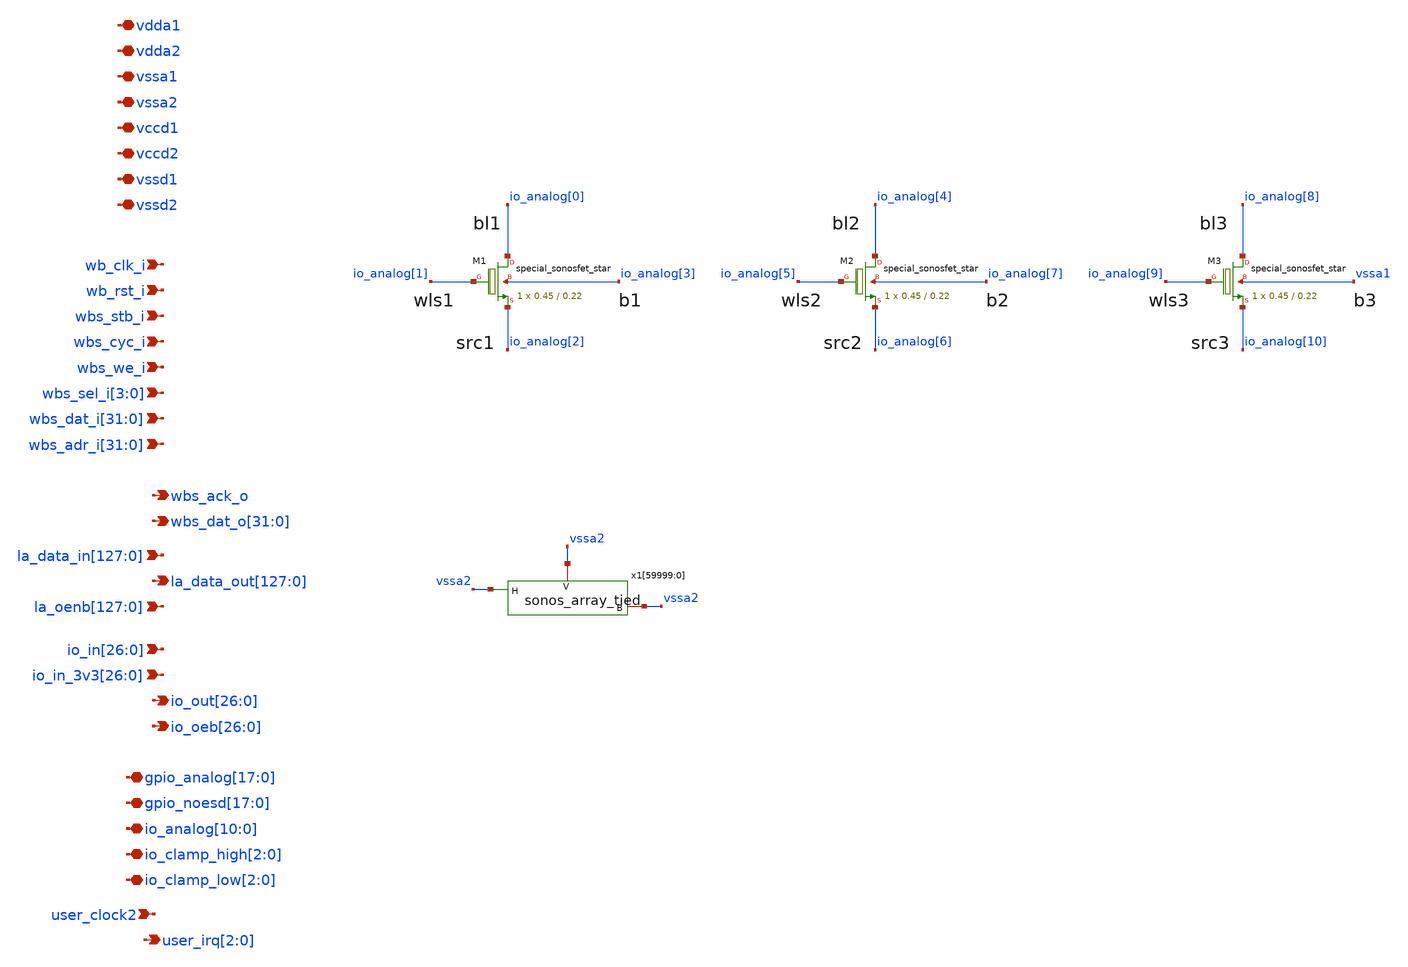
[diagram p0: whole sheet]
** sch_path: xschem/user_analog_project_wrapper.sch
**.subckt user_analog_project_wrapper vdda1 vdda2 vssa1 vssa2 vccd1 vccd2 vssd1 vssd2 wb_clk_i
*+ wb_rst_i wbs_stb_i wbs_cyc_i wbs_we_i wbs_sel_i[3],wbs_sel_i[2],wbs_sel_i[1],wbs_sel_i[0]
*+ wbs_dat_i[31],wbs_dat_i[30],wbs_dat_i[29],wbs_dat_i[28],wbs_dat_i[27],wbs_dat_i[26],wbs_dat_i[25],wbs_dat_i[24],wbs_dat_i[23],wbs_dat_i[22],wbs_dat_i[21],wbs_dat_i[20],wbs_dat_i[19],wbs_dat_i[18],wbs_dat_i[17],wbs_dat_i[16],wbs_dat_i[15],wbs_dat_i[14],wbs_dat_i[13],wbs_dat_i[12],wbs_dat_i[11],wbs_dat_i[10],wbs_dat_i[9],wbs_dat_i[8],wbs_dat_i[7],wbs_dat_i[6],wbs_dat_i[5],wbs_dat_i[4],wbs_dat_i[3],wbs_dat_i[2],wbs_dat_i[1],wbs_dat_i[0]
*+ wbs_adr_i[31],wbs_adr_i[30],wbs_adr_i[29],wbs_adr_i[28],wbs_adr_i[27],wbs_adr_i[26],wbs_adr_i[25],wbs_adr_i[24],wbs_adr_i[23],wbs_adr_i[22],wbs_adr_i[21],wbs_adr_i[20],wbs_adr_i[19],wbs_adr_i[18],wbs_adr_i[17],wbs_adr_i[16],wbs_adr_i[15],wbs_adr_i[14],wbs_adr_i[13],wbs_adr_i[12],wbs_adr_i[11],wbs_adr_i[10],wbs_adr_i[9],wbs_adr_i[8],wbs_adr_i[7],wbs_adr_i[6],wbs_adr_i[5],wbs_adr_i[4],wbs_adr_i[3],wbs_adr_i[2],wbs_adr_i[1],wbs_adr_i[0] wbs_ack_o
*+ wbs_dat_o[31],wbs_dat_o[30],wbs_dat_o[29],wbs_dat_o[28],wbs_dat_o[27],wbs_dat_o[26],wbs_dat_o[25],wbs_dat_o[24],wbs_dat_o[23],wbs_dat_o[22],wbs_dat_o[21],wbs_dat_o[20],wbs_dat_o[19],wbs_dat_o[18],wbs_dat_o[17],wbs_dat_o[16],wbs_dat_o[15],wbs_dat_o[14],wbs_dat_o[13],wbs_dat_o[12],wbs_dat_o[11],wbs_dat_o[10],wbs_dat_o[9],wbs_dat_o[8],wbs_dat_o[7],wbs_dat_o[6],wbs_dat_o[5],wbs_dat_o[4],wbs_dat_o[3],wbs_dat_o[2],wbs_dat_o[1],wbs_dat_o[0]
*+ la_data_in[127],la_data_in[126],la_data_in[125],la_data_in[124],la_data_in[123],la_data_in[122],la_data_in[121],la_data_in[120],la_data_in[119],la_data_in[118],la_data_in[117],la_data_in[116],la_data_in[115],la_data_in[114],la_data_in[113],la_data_in[112],la_data_in[111],la_data_in[110],la_data_in[109],la_data_in[108],la_data_in[107],la_data_in[106],la_data_in[105],la_data_in[104],la_data_in[103],la_data_in[102],la_data_in[101],la_data_in[100],la_data_in[99],la_data_in[98],la_data_in[97],la_data_in[96],la_data_in[95],la_data_in[94],la_data_in[93],la_data_in[92],la_data_in[91],la_data_in[90],la_data_in[89],la_data_in[88],la_data_in[87],la_data_in[86],la_data_in[85],la_data_in[84],la_data_in[83],la_data_in[82],la_data_in[81],la_data_in[80],la_data_in[79],la_data_in[78],la_data_in[77],la_data_in[76],la_data_in[75],la_data_in[74],la_data_in[73],la_data_in[72],la_data_in[71],la_data_in[70],la_data_in[69],la_data_in[68],la_data_in[67],la_data_in[66],la_data_in[65],la_data_in[64],la_data_in[63],la_data_in[62],la_data_in[61],la_data_in[60],la_data_in[59],la_data_in[58],la_data_in[57],la_data_in[56],la_data_in[55],la_data_in[54],la_data_in[53],la_data_in[52],la_data_in[51],la_data_in[50],la_data_in[49],la_data_in[48],la_data_in[47],la_data_in[46],la_data_in[45],la_data_in[44],la_data_in[43],la_data_in[42],la_data_in[41],la_data_in[40],la_data_in[39],la_data_in[38],la_data_in[37],la_data_in[36],la_data_in[35],la_data_in[34],la_data_in[33],la_data_in[32],la_data_in[31],la_data_in[30],la_data_in[29],la_data_in[28],la_data_in[27],la_data_in[26],la_data_in[25],la_data_in[24],la_data_in[23],la_data_in[22],la_data_in[21],la_data_in[20],la_data_in[19],la_data_in[18],la_data_in[17],la_data_in[16],la_data_in[15],la_data_in[14],la_data_in[13],la_data_in[12],la_data_in[11],la_data_in[10],la_data_in[9],la_data_in[8],la_data_in[7],la_data_in[6],la_data_in[5],la_data_in[4],la_data_in[3],la_data_in[2],la_data_in[1],la_data_in[0]
*+ la_data_out[127],la_data_out[126],la_data_out[125],la_data_out[124],la_data_out[123],la_data_out[122],la_data_out[121],la_data_out[120],la_data_out[119],la_data_out[118],la_data_out[117],la_data_out[116],la_data_out[115],la_data_out[114],la_data_out[113],la_data_out[112],la_data_out[111],la_data_out[110],la_data_out[109],la_data_out[108],la_data_out[107],la_data_out[106],la_data_out[105],la_data_out[104],la_data_out[103],la_data_out[102],la_data_out[101],la_data_out[100],la_data_out[99],la_data_out[98],la_data_out[97],la_data_out[96],la_data_out[95],la_data_out[94],la_data_out[93],la_data_out[92],la_data_out[91],la_data_out[90],la_data_out[89],la_data_out[88],la_data_out[87],la_data_out[86],la_data_out[85],la_data_out[84],la_data_out[83],la_data_out[82],la_data_out[81],la_data_out[80],la_data_out[79],la_data_out[78],la_data_out[77],la_data_out[76],la_data_out[75],la_data_out[74],la_data_out[73],la_data_out[72],la_data_out[71],la_data_out[70],la_data_out[69],la_data_out[68],la_data_out[67],la_data_out[66],la_data_out[65],la_data_out[64],la_data_out[63],la_data_out[62],la_data_out[61],la_data_out[60],la_data_out[59],la_data_out[58],la_data_out[57],la_data_out[56],la_data_out[55],la_data_out[54],la_data_out[53],la_data_out[52],la_data_out[51],la_data_out[50],la_data_out[49],la_data_out[48],la_data_out[47],la_data_out[46],la_data_out[45],la_data_out[44],la_data_out[43],la_data_out[42],la_data_out[41],la_data_out[40],la_data_out[39],la_data_out[38],la_data_out[37],la_data_out[36],la_data_out[35],la_data_out[34],la_data_out[33],la_data_out[32],la_data_out[31],la_data_out[30],la_data_out[29],la_data_out[28],la_data_out[27],la_data_out[26],la_data_out[25],la_data_out[24],la_data_out[23],la_data_out[22],la_data_out[21],la_data_out[20],la_data_out[19],la_data_out[18],la_data_out[17],la_data_out[16],la_data_out[15],la_data_out[14],la_data_out[13],la_data_out[12],la_data_out[11],la_data_out[10],la_data_out[9],la_data_out[8],la_data_out[7],la_data_out[6],la_data_out[5],la_data_out[4],la_data_out[3],la_data_out[2],la_data_out[1],la_data_out[0]
*+ io_in[26],io_in[25],io_in[24],io_in[23],io_in[22],io_in[21],io_in[20],io_in[19],io_in[18],io_in[17],io_in[16],io_in[15],io_in[14],io_in[13],io_in[12],io_in[11],io_in[10],io_in[9],io_in[8],io_in[7],io_in[6],io_in[5],io_in[4],io_in[3],io_in[2],io_in[1],io_in[0]
*+ io_in_3v3[26],io_in_3v3[25],io_in_3v3[24],io_in_3v3[23],io_in_3v3[22],io_in_3v3[21],io_in_3v3[20],io_in_3v3[19],io_in_3v3[18],io_in_3v3[17],io_in_3v3[16],io_in_3v3[15],io_in_3v3[14],io_in_3v3[13],io_in_3v3[12],io_in_3v3[11],io_in_3v3[10],io_in_3v3[9],io_in_3v3[8],io_in_3v3[7],io_in_3v3[6],io_in_3v3[5],io_in_3v3[4],io_in_3v3[3],io_in_3v3[2],io_in_3v3[1],io_in_3v3[0] user_clock2
*+ io_out[26],io_out[25],io_out[24],io_out[23],io_out[22],io_out[21],io_out[20],io_out[19],io_out[18],io_out[17],io_out[16],io_out[15],io_out[14],io_out[13],io_out[12],io_out[11],io_out[10],io_out[9],io_out[8],io_out[7],io_out[6],io_out[5],io_out[4],io_out[3],io_out[2],io_out[1],io_out[0]
*+ io_oeb[26],io_oeb[25],io_oeb[24],io_oeb[23],io_oeb[22],io_oeb[21],io_oeb[20],io_oeb[19],io_oeb[18],io_oeb[17],io_oeb[16],io_oeb[15],io_oeb[14],io_oeb[13],io_oeb[12],io_oeb[11],io_oeb[10],io_oeb[9],io_oeb[8],io_oeb[7],io_oeb[6],io_oeb[5],io_oeb[4],io_oeb[3],io_oeb[2],io_oeb[1],io_oeb[0]
*+ gpio_analog[17],gpio_analog[16],gpio_analog[15],gpio_analog[14],gpio_analog[13],gpio_analog[12],gpio_analog[11],gpio_analog[10],gpio_analog[9],gpio_analog[8],gpio_analog[7],gpio_analog[6],gpio_analog[5],gpio_analog[4],gpio_analog[3],gpio_analog[2],gpio_analog[1],gpio_analog[0]
*+ gpio_noesd[17],gpio_noesd[16],gpio_noesd[15],gpio_noesd[14],gpio_noesd[13],gpio_noesd[12],gpio_noesd[11],gpio_noesd[10],gpio_noesd[9],gpio_noesd[8],gpio_noesd[7],gpio_noesd[6],gpio_noesd[5],gpio_noesd[4],gpio_noesd[3],gpio_noesd[2],gpio_noesd[1],gpio_noesd[0]
*+ io_analog[10],io_analog[9],io_analog[8],io_analog[7],io_analog[6],io_analog[5],io_analog[4],io_analog[3],io_analog[2],io_analog[1],io_analog[0] io_clamp_high[2],io_clamp_high[1],io_clamp_high[0] io_clamp_low[2],io_clamp_low[1],io_clamp_low[0]
*+ user_irq[2],user_irq[1],user_irq[0]
*+ la_oenb[127],la_oenb[126],la_oenb[125],la_oenb[124],la_oenb[123],la_oenb[122],la_oenb[121],la_oenb[120],la_oenb[119],la_oenb[118],la_oenb[117],la_oenb[116],la_oenb[115],la_oenb[114],la_oenb[113],la_oenb[112],la_oenb[111],la_oenb[110],la_oenb[109],la_oenb[108],la_oenb[107],la_oenb[106],la_oenb[105],la_oenb[104],la_oenb[103],la_oenb[102],la_oenb[101],la_oenb[100],la_oenb[99],la_oenb[98],la_oenb[97],la_oenb[96],la_oenb[95],la_oenb[94],la_oenb[93],la_oenb[92],la_oenb[91],la_oenb[90],la_oenb[89],la_oenb[88],la_oenb[87],la_oenb[86],la_oenb[85],la_oenb[84],la_oenb[83],la_oenb[82],la_oenb[81],la_oenb[80],la_oenb[79],la_oenb[78],la_oenb[77],la_oenb[76],la_oenb[75],la_oenb[74],la_oenb[73],la_oenb[72],la_oenb[71],la_oenb[70],la_oenb[69],la_oenb[68],la_oenb[67],la_oenb[66],la_oenb[65],la_oenb[64],la_oenb[63],la_oenb[62],la_oenb[61],la_oenb[60],la_oenb[59],la_oenb[58],la_oenb[57],la_oenb[56],la_oenb[55],la_oenb[54],la_oenb[53],la_oenb[52],la_oenb[51],la_oenb[50],la_oenb[49],la_oenb[48],la_oenb[47],la_oenb[46],la_oenb[45],la_oenb[44],la_oenb[43],la_oenb[42],la_oenb[41],la_oenb[40],la_oenb[39],la_oenb[38],la_oenb[37],la_oenb[36],la_oenb[35],la_oenb[34],la_oenb[33],la_oenb[32],la_oenb[31],la_oenb[30],la_oenb[29],la_oenb[28],la_oenb[27],la_oenb[26],la_oenb[25],la_oenb[24],la_oenb[23],la_oenb[22],la_oenb[21],la_oenb[20],la_oenb[19],la_oenb[18],la_oenb[17],la_oenb[16],la_oenb[15],la_oenb[14],la_oenb[13],la_oenb[12],la_oenb[11],la_oenb[10],la_oenb[9],la_oenb[8],la_oenb[7],la_oenb[6],la_oenb[5],la_oenb[4],la_oenb[3],la_oenb[2],la_oenb[1],la_oenb[0]
*.iopin vdda1
*.iopin vdda2
*.iopin vssa1
*.iopin vssa2
*.iopin vccd1
*.iopin vccd2
*.iopin vssd1
*.iopin vssd2
*.ipin wb_clk_i
*.ipin wb_rst_i
*.ipin wbs_stb_i
*.ipin wbs_cyc_i
*.ipin wbs_we_i
*.ipin wbs_sel_i[3],wbs_sel_i[2],wbs_sel_i[1],wbs_sel_i[0]
*.ipin
*+ wbs_dat_i[31],wbs_dat_i[30],wbs_dat_i[29],wbs_dat_i[28],wbs_dat_i[27],wbs_dat_i[26],wbs_dat_i[25],wbs_dat_i[24],wbs_dat_i[23],wbs_dat_i[22],wbs_dat_i[21],wbs_dat_i[20],wbs_dat_i[19],wbs_dat_i[18],wbs_dat_i[17],wbs_dat_i[16],wbs_dat_i[15],wbs_dat_i[14],wbs_dat_i[13],wbs_dat_i[12],wbs_dat_i[11],wbs_dat_i[10],wbs_dat_i[9],wbs_dat_i[8],wbs_dat_i[7],wbs_dat_i[6],wbs_dat_i[5],wbs_dat_i[4],wbs_dat_i[3],wbs_dat_i[2],wbs_dat_i[1],wbs_dat_i[0]
*.ipin
*+ wbs_adr_i[31],wbs_adr_i[30],wbs_adr_i[29],wbs_adr_i[28],wbs_adr_i[27],wbs_adr_i[26],wbs_adr_i[25],wbs_adr_i[24],wbs_adr_i[23],wbs_adr_i[22],wbs_adr_i[21],wbs_adr_i[20],wbs_adr_i[19],wbs_adr_i[18],wbs_adr_i[17],wbs_adr_i[16],wbs_adr_i[15],wbs_adr_i[14],wbs_adr_i[13],wbs_adr_i[12],wbs_adr_i[11],wbs_adr_i[10],wbs_adr_i[9],wbs_adr_i[8],wbs_adr_i[7],wbs_adr_i[6],wbs_adr_i[5],wbs_adr_i[4],wbs_adr_i[3],wbs_adr_i[2],wbs_adr_i[1],wbs_adr_i[0]
*.opin wbs_ack_o
*.opin
*+ wbs_dat_o[31],wbs_dat_o[30],wbs_dat_o[29],wbs_dat_o[28],wbs_dat_o[27],wbs_dat_o[26],wbs_dat_o[25],wbs_dat_o[24],wbs_dat_o[23],wbs_dat_o[22],wbs_dat_o[21],wbs_dat_o[20],wbs_dat_o[19],wbs_dat_o[18],wbs_dat_o[17],wbs_dat_o[16],wbs_dat_o[15],wbs_dat_o[14],wbs_dat_o[13],wbs_dat_o[12],wbs_dat_o[11],wbs_dat_o[10],wbs_dat_o[9],wbs_dat_o[8],wbs_dat_o[7],wbs_dat_o[6],wbs_dat_o[5],wbs_dat_o[4],wbs_dat_o[3],wbs_dat_o[2],wbs_dat_o[1],wbs_dat_o[0]
*.ipin
*+ la_data_in[127],la_data_in[126],la_data_in[125],la_data_in[124],la_data_in[123],la_data_in[122],la_data_in[121],la_data_in[120],la_data_in[119],la_data_in[118],la_data_in[117],la_data_in[116],la_data_in[115],la_data_in[114],la_data_in[113],la_data_in[112],la_data_in[111],la_data_in[110],la_data_in[109],la_data_in[108],la_data_in[107],la_data_in[106],la_data_in[105],la_data_in[104],la_data_in[103],la_data_in[102],la_data_in[101],la_data_in[100],la_data_in[99],la_data_in[98],la_data_in[97],la_data_in[96],la_data_in[95],la_data_in[94],la_data_in[93],la_data_in[92],la_data_in[91],la_data_in[90],la_data_in[89],la_data_in[88],la_data_in[87],la_data_in[86],la_data_in[85],la_data_in[84],la_data_in[83],la_data_in[82],la_data_in[81],la_data_in[80],la_data_in[79],la_data_in[78],la_data_in[77],la_data_in[76],la_data_in[75],la_data_in[74],la_data_in[73],la_data_in[72],la_data_in[71],la_data_in[70],la_data_in[69],la_data_in[68],la_data_in[67],la_data_in[66],la_data_in[65],la_data_in[64],la_data_in[63],la_data_in[62],la_data_in[61],la_data_in[60],la_data_in[59],la_data_in[58],la_data_in[57],la_data_in[56],la_data_in[55],la_data_in[54],la_data_in[53],la_data_in[52],la_data_in[51],la_data_in[50],la_data_in[49],la_data_in[48],la_data_in[47],la_data_in[46],la_data_in[45],la_data_in[44],la_data_in[43],la_data_in[42],la_data_in[41],la_data_in[40],la_data_in[39],la_data_in[38],la_data_in[37],la_data_in[36],la_data_in[35],la_data_in[34],la_data_in[33],la_data_in[32],la_data_in[31],la_data_in[30],la_data_in[29],la_data_in[28],la_data_in[27],la_data_in[26],la_data_in[25],la_data_in[24],la_data_in[23],la_data_in[22],la_data_in[21],la_data_in[20],la_data_in[19],la_data_in[18],la_data_in[17],la_data_in[16],la_data_in[15],la_data_in[14],la_data_in[13],la_data_in[12],la_data_in[11],la_data_in[10],la_data_in[9],la_data_in[8],la_data_in[7],la_data_in[6],la_data_in[5],la_data_in[4],la_data_in[3],la_data_in[2],la_data_in[1],la_data_in[0]
*.opin
*+ la_data_out[127],la_data_out[126],la_data_out[125],la_data_out[124],la_data_out[123],la_data_out[122],la_data_out[121],la_data_out[120],la_data_out[119],la_data_out[118],la_data_out[117],la_data_out[116],la_data_out[115],la_data_out[114],la_data_out[113],la_data_out[112],la_data_out[111],la_data_out[110],la_data_out[109],la_data_out[108],la_data_out[107],la_data_out[106],la_data_out[105],la_data_out[104],la_data_out[103],la_data_out[102],la_data_out[101],la_data_out[100],la_data_out[99],la_data_out[98],la_data_out[97],la_data_out[96],la_data_out[95],la_data_out[94],la_data_out[93],la_data_out[92],la_data_out[91],la_data_out[90],la_data_out[89],la_data_out[88],la_data_out[87],la_data_out[86],la_data_out[85],la_data_out[84],la_data_out[83],la_data_out[82],la_data_out[81],la_data_out[80],la_data_out[79],la_data_out[78],la_data_out[77],la_data_out[76],la_data_out[75],la_data_out[74],la_data_out[73],la_data_out[72],la_data_out[71],la_data_out[70],la_data_out[69],la_data_out[68],la_data_out[67],la_data_out[66],la_data_out[65],la_data_out[64],la_data_out[63],la_data_out[62],la_data_out[61],la_data_out[60],la_data_out[59],la_data_out[58],la_data_out[57],la_data_out[56],la_data_out[55],la_data_out[54],la_data_out[53],la_data_out[52],la_data_out[51],la_data_out[50],la_data_out[49],la_data_out[48],la_data_out[47],la_data_out[46],la_data_out[45],la_data_out[44],la_data_out[43],la_data_out[42],la_data_out[41],la_data_out[40],la_data_out[39],la_data_out[38],la_data_out[37],la_data_out[36],la_data_out[35],la_data_out[34],la_data_out[33],la_data_out[32],la_data_out[31],la_data_out[30],la_data_out[29],la_data_out[28],la_data_out[27],la_data_out[26],la_data_out[25],la_data_out[24],la_data_out[23],la_data_out[22],la_data_out[21],la_data_out[20],la_data_out[19],la_data_out[18],la_data_out[17],la_data_out[16],la_data_out[15],la_data_out[14],la_data_out[13],la_data_out[12],la_data_out[11],la_data_out[10],la_data_out[9],la_data_out[8],la_data_out[7],la_data_out[6],la_data_out[5],la_data_out[4],la_data_out[3],la_data_out[2],la_data_out[1],la_data_out[0]
*.ipin
*+ io_in[26],io_in[25],io_in[24],io_in[23],io_in[22],io_in[21],io_in[20],io_in[19],io_in[18],io_in[17],io_in[16],io_in[15],io_in[14],io_in[13],io_in[12],io_in[11],io_in[10],io_in[9],io_in[8],io_in[7],io_in[6],io_in[5],io_in[4],io_in[3],io_in[2],io_in[1],io_in[0]
*.ipin
*+ io_in_3v3[26],io_in_3v3[25],io_in_3v3[24],io_in_3v3[23],io_in_3v3[22],io_in_3v3[21],io_in_3v3[20],io_in_3v3[19],io_in_3v3[18],io_in_3v3[17],io_in_3v3[16],io_in_3v3[15],io_in_3v3[14],io_in_3v3[13],io_in_3v3[12],io_in_3v3[11],io_in_3v3[10],io_in_3v3[9],io_in_3v3[8],io_in_3v3[7],io_in_3v3[6],io_in_3v3[5],io_in_3v3[4],io_in_3v3[3],io_in_3v3[2],io_in_3v3[1],io_in_3v3[0]
*.ipin user_clock2
*.opin
*+ io_out[26],io_out[25],io_out[24],io_out[23],io_out[22],io_out[21],io_out[20],io_out[19],io_out[18],io_out[17],io_out[16],io_out[15],io_out[14],io_out[13],io_out[12],io_out[11],io_out[10],io_out[9],io_out[8],io_out[7],io_out[6],io_out[5],io_out[4],io_out[3],io_out[2],io_out[1],io_out[0]
*.opin
*+ io_oeb[26],io_oeb[25],io_oeb[24],io_oeb[23],io_oeb[22],io_oeb[21],io_oeb[20],io_oeb[19],io_oeb[18],io_oeb[17],io_oeb[16],io_oeb[15],io_oeb[14],io_oeb[13],io_oeb[12],io_oeb[11],io_oeb[10],io_oeb[9],io_oeb[8],io_oeb[7],io_oeb[6],io_oeb[5],io_oeb[4],io_oeb[3],io_oeb[2],io_oeb[1],io_oeb[0]
*.iopin
*+ gpio_analog[17],gpio_analog[16],gpio_analog[15],gpio_analog[14],gpio_analog[13],gpio_analog[12],gpio_analog[11],gpio_analog[10],gpio_analog[9],gpio_analog[8],gpio_analog[7],gpio_analog[6],gpio_analog[5],gpio_analog[4],gpio_analog[3],gpio_analog[2],gpio_analog[1],gpio_analog[0]
*.iopin
*+ gpio_noesd[17],gpio_noesd[16],gpio_noesd[15],gpio_noesd[14],gpio_noesd[13],gpio_noesd[12],gpio_noesd[11],gpio_noesd[10],gpio_noesd[9],gpio_noesd[8],gpio_noesd[7],gpio_noesd[6],gpio_noesd[5],gpio_noesd[4],gpio_noesd[3],gpio_noesd[2],gpio_noesd[1],gpio_noesd[0]
*.iopin
*+ io_analog[10],io_analog[9],io_analog[8],io_analog[7],io_analog[6],io_analog[5],io_analog[4],io_analog[3],io_analog[2],io_analog[1],io_analog[0]
*.iopin io_clamp_high[2],io_clamp_high[1],io_clamp_high[0]
*.iopin io_clamp_low[2],io_clamp_low[1],io_clamp_low[0]
*.opin user_irq[2],user_irq[1],user_irq[0]
*.ipin
*+ la_oenb[127],la_oenb[126],la_oenb[125],la_oenb[124],la_oenb[123],la_oenb[122],la_oenb[121],la_oenb[120],la_oenb[119],la_oenb[118],la_oenb[117],la_oenb[116],la_oenb[115],la_oenb[114],la_oenb[113],la_oenb[112],la_oenb[111],la_oenb[110],la_oenb[109],la_oenb[108],la_oenb[107],la_oenb[106],la_oenb[105],la_oenb[104],la_oenb[103],la_oenb[102],la_oenb[101],la_oenb[100],la_oenb[99],la_oenb[98],la_oenb[97],la_oenb[96],la_oenb[95],la_oenb[94],la_oenb[93],la_oenb[92],la_oenb[91],la_oenb[90],la_oenb[89],la_oenb[88],la_oenb[87],la_oenb[86],la_oenb[85],la_oenb[84],la_oenb[83],la_oenb[82],la_oenb[81],la_oenb[80],la_oenb[79],la_oenb[78],la_oenb[77],la_oenb[76],la_oenb[75],la_oenb[74],la_oenb[73],la_oenb[72],la_oenb[71],la_oenb[70],la_oenb[69],la_oenb[68],la_oenb[67],la_oenb[66],la_oenb[65],la_oenb[64],la_oenb[63],la_oenb[62],la_oenb[61],la_oenb[60],la_oenb[59],la_oenb[58],la_oenb[57],la_oenb[56],la_oenb[55],la_oenb[54],la_oenb[53],la_oenb[52],la_oenb[51],la_oenb[50],la_oenb[49],la_oenb[48],la_oenb[47],la_oenb[46],la_oenb[45],la_oenb[44],la_oenb[43],la_oenb[42],la_oenb[41],la_oenb[40],la_oenb[39],la_oenb[38],la_oenb[37],la_oenb[36],la_oenb[35],la_oenb[34],la_oenb[33],la_oenb[32],la_oenb[31],la_oenb[30],la_oenb[29],la_oenb[28],la_oenb[27],la_oenb[26],la_oenb[25],la_oenb[24],la_oenb[23],la_oenb[22],la_oenb[21],la_oenb[20],la_oenb[19],la_oenb[18],la_oenb[17],la_oenb[16],la_oenb[15],la_oenb[14],la_oenb[13],la_oenb[12],la_oenb[11],la_oenb[10],la_oenb[9],la_oenb[8],la_oenb[7],la_oenb[6],la_oenb[5],la_oenb[4],la_oenb[3],la_oenb[2],la_oenb[1],la_oenb[0]
XM1 io_analog[0] io_analog[1] io_analog[2] io_analog[3] sky130_fd_bs__special_sonosfet_star L=0.22
+ W=0.45 m=1
XM2 io_analog[4] io_analog[5] io_analog[6] io_analog[7] sky130_fd_bs__special_sonosfet_star L=0.22
+ W=0.45 m=1
XM3 io_analog[8] io_analog[9] io_analog[10] vssa1 sky130_fd_bs__special_sonosfet_star L=0.22 W=0.45
+ m=1
x1[59999:0] vssa2 vssa2 vssa2 sonos_array_tied
**.ends

* expanding   symbol:  sonos_array_tied.sym # of pins=3
** sym_path: xschem/sonos_array_tied.sym
** sch_path: xschem/sonos_array_tied.sch
.subckt sonos_array_tied V H B
*.ipin H
*.iopin V
*.iopin B
X1 H H H H H H H H H H H H H H H H V V V V V V V V V V V V V V V V B sonos_array
.ends


* expanding   symbol:  sonos_array.sym # of pins=33
** sym_path: xschem/sonos_array.sym
** sch_path: xschem/sonos_array.sch
.subckt sonos_array WLS3 WL1 WL4 WLS4 WL6 WLS1 WL7 WL0 WL5 WLS5 WLS0 WL2 WLS2 WLS6 WL3 WLS7 BL0 SRC0
+ BL1 SRC1 BL2 SRC2 BL3 SRC3 BL4 SRC4 BL5 SRC5 BL6 SRC6 BL7 SRC7 BODY
*.iopin BL0
*.ipin WL0
*.ipin WLS0
*.ipin WL1
*.ipin WLS1
*.ipin WL2
*.ipin WLS2
*.ipin WL3
*.ipin WLS3
*.ipin WL4
*.ipin WLS4
*.ipin WL5
*.ipin WLS5
*.ipin WL6
*.ipin WLS6
*.ipin WL7
*.ipin WLS7
*.iopin BL1
*.iopin BL2
*.iopin BL3
*.iopin BL4
*.iopin BL5
*.iopin BL6
*.iopin BL7
*.iopin SRC0
*.iopin SRC1
*.iopin SRC2
*.iopin SRC3
*.iopin SRC4
*.iopin SRC5
*.iopin SRC6
*.iopin SRC7
*.iopin BODY
x1 BL0 WLS0 BODY WL0 SRC0 sonos_cell
x2 BL1 WLS0 BODY WL0 SRC1 sonos_cell
x3 BL2 WLS0 BODY WL0 SRC2 sonos_cell
x4 BL3 WLS0 BODY WL0 SRC3 sonos_cell
x5 BL4 WLS0 BODY WL0 SRC4 sonos_cell
x6 BL5 WLS0 BODY WL0 SRC5 sonos_cell
x7 BL6 WLS0 BODY WL0 SRC6 sonos_cell
x8 BL7 WLS0 BODY WL0 SRC7 sonos_cell
x9 BL0 WLS1 BODY WL1 SRC0 sonos_cell
x10 BL1 WLS1 BODY WL1 SRC1 sonos_cell
x11 BL2 WLS1 BODY WL1 SRC2 sonos_cell
x12 BL3 WLS1 BODY WL1 SRC3 sonos_cell
x13 BL4 WLS1 BODY WL1 SRC4 sonos_cell
x14 BL5 WLS1 BODY WL1 SRC5 sonos_cell
x15 BL6 WLS1 BODY WL1 SRC6 sonos_cell
x16 BL7 WLS1 BODY WL1 SRC7 sonos_cell
x17 BL0 WLS2 BODY WL2 SRC0 sonos_cell
x18 BL1 WLS2 BODY WL2 SRC1 sonos_cell
x19 BL2 WLS2 BODY WL2 SRC2 sonos_cell
x20 BL3 WLS2 BODY WL2 SRC3 sonos_cell
x21 BL4 WLS2 BODY WL2 SRC4 sonos_cell
x22 BL5 WLS2 BODY WL2 SRC5 sonos_cell
x23 BL6 WLS2 BODY WL2 SRC6 sonos_cell
x24 BL7 WLS2 BODY WL2 SRC7 sonos_cell
x25 BL0 WLS3 BODY WL3 SRC0 sonos_cell
x26 BL1 WLS3 BODY WL3 SRC1 sonos_cell
x27 BL2 WLS3 BODY WL3 SRC2 sonos_cell
x28 BL3 WLS3 BODY WL3 SRC3 sonos_cell
x29 BL4 WLS3 BODY WL3 SRC4 sonos_cell
x30 BL5 WLS3 BODY WL3 SRC5 sonos_cell
x31 BL6 WLS3 BODY WL3 SRC6 sonos_cell
x32 BL7 WLS3 BODY WL3 SRC7 sonos_cell
x33 BL0 WLS4 BODY WL4 SRC0 sonos_cell
x34 BL1 WLS4 BODY WL4 SRC1 sonos_cell
x35 BL2 WLS4 BODY WL4 SRC2 sonos_cell
x36 BL3 WLS4 BODY WL4 SRC3 sonos_cell
x37 BL4 WLS4 BODY WL4 SRC4 sonos_cell
x38 BL5 WLS4 BODY WL4 SRC5 sonos_cell
x39 BL6 WLS4 BODY WL4 SRC6 sonos_cell
x40 BL7 WLS4 BODY WL4 SRC7 sonos_cell
x41 BL0 WLS5 BODY WL5 SRC0 sonos_cell
x42 BL1 WLS5 BODY WL5 SRC1 sonos_cell
x43 BL2 WLS5 BODY WL5 SRC2 sonos_cell
x44 BL3 WLS5 BODY WL5 SRC3 sonos_cell
x45 BL4 WLS5 BODY WL5 SRC4 sonos_cell
x46 BL5 WLS5 BODY WL5 SRC5 sonos_cell
x47 BL6 WLS5 BODY WL5 SRC6 sonos_cell
x48 BL7 WLS5 BODY WL5 SRC7 sonos_cell
x49 BL0 WLS6 BODY WL6 SRC0 sonos_cell
x50 BL1 WLS6 BODY WL6 SRC1 sonos_cell
x51 BL2 WLS6 BODY WL6 SRC2 sonos_cell
x52 BL3 WLS6 BODY WL6 SRC3 sonos_cell
x53 BL4 WLS6 BODY WL6 SRC4 sonos_cell
x54 BL5 WLS6 BODY WL6 SRC5 sonos_cell
x55 BL6 WLS6 BODY WL6 SRC6 sonos_cell
x56 BL7 WLS6 BODY WL6 SRC7 sonos_cell
x57 BL0 WLS7 BODY WL7 SRC0 sonos_cell
x58 BL1 WLS7 BODY WL7 SRC1 sonos_cell
x59 BL2 WLS7 BODY WL7 SRC2 sonos_cell
x60 BL3 WLS7 BODY WL7 SRC3 sonos_cell
x61 BL4 WLS7 BODY WL7 SRC4 sonos_cell
x62 BL5 WLS7 BODY WL7 SRC5 sonos_cell
x63 BL6 WLS7 BODY WL7 SRC6 sonos_cell
x64 BL7 WLS7 BODY WL7 SRC7 sonos_cell
.ends


* expanding   symbol:  sonos_cell.sym # of pins=5
** sym_path: xschem/sonos_cell.sym
** sch_path: xschem/sonos_cell.sch
.subckt sonos_cell BL WLS B WL SRC
*.ipin WLS
*.ipin WL
*.iopin B
*.iopin BL
*.iopin SRC
XM1 BL WLS net1 B sky130_fd_bs__special_sonosfet_star L=0.22 W=0.45 m=1
XM2 net1 WL SRC B sky130_fd_bs__special_nfet_pass_flash L=0.15 W=0.45 m=1
.ends

.end
